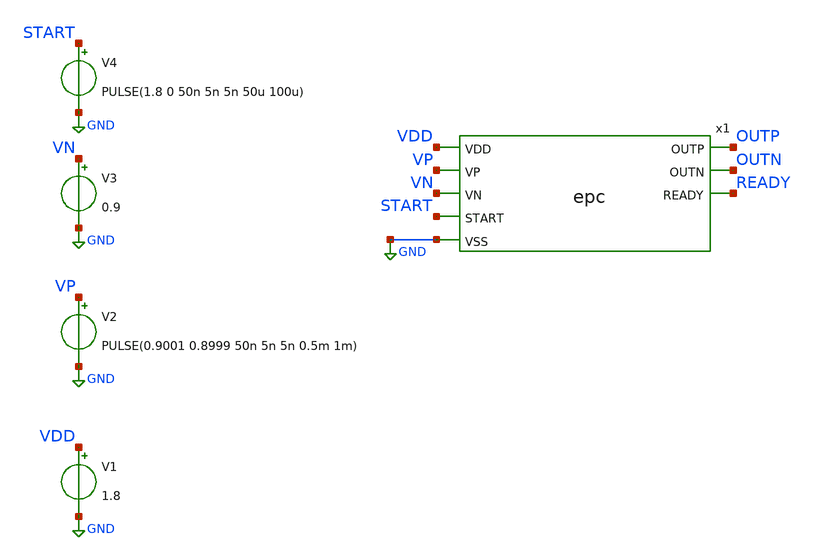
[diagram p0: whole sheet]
** sch_path: xschem/schematics/epc_tb.sch
**.subckt epc_tb
x1 VDD OUTP VP OUTN VN READY START GND epc
V1 VDD GND 1.8
V2 VP GND PULSE(0.9001 0.8999 50n 5n 5n 0.5m 1m)
V3 VN GND 0.9
V4 START GND PULSE(1.8 0 50n 5n 5n 50u 100u)
**** begin user architecture code

** opencircuitdesign pdks install
.lib $::SKYWATER_MODELS/sky130.lib.spice tt
.include /usr/local/share/pdk/sky130A/libs.ref/sky130_fd_sc_hd/spice/sky130_fd_sc_hd.spice



.option wnflag=0
.option savecurrents
.control
tran 1m 1m
plot V(vp) V(vn)
plot V(outp)
plot V(outn)
plot V(ready)
.endc

**** end user architecture code
**.ends
.GLOBAL GND
.end
